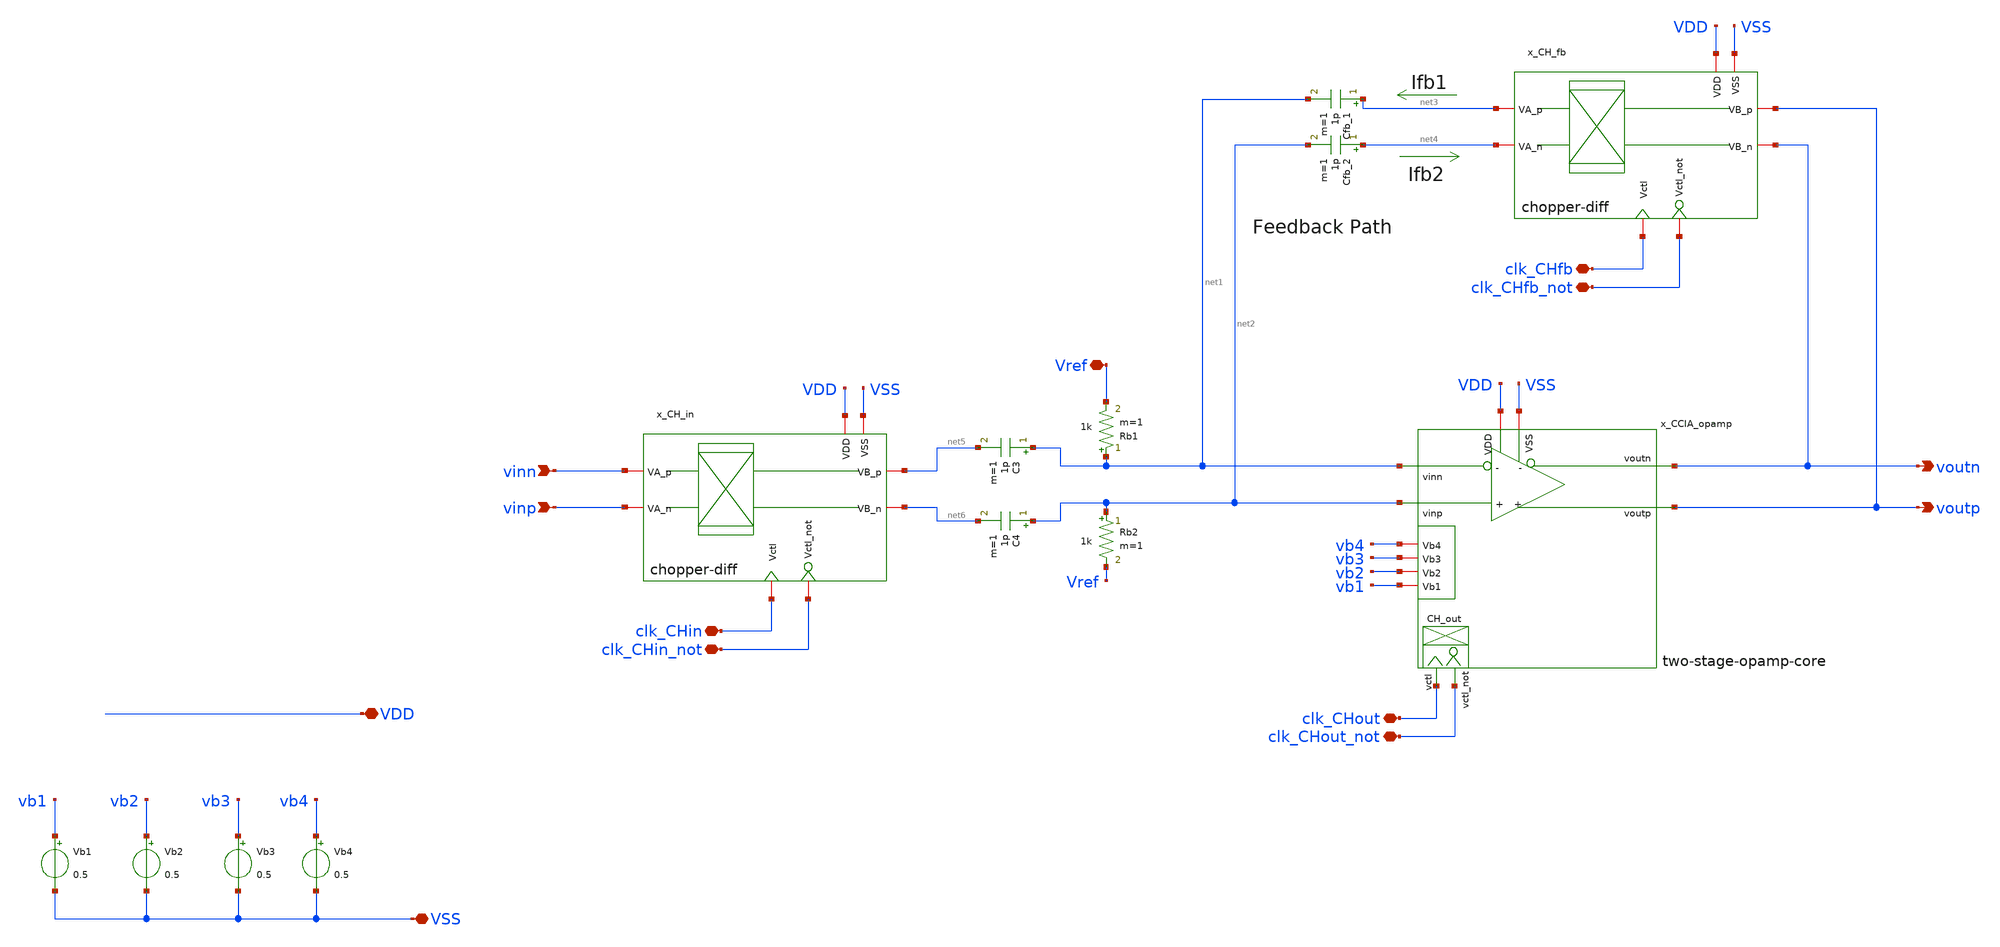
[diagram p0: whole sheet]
** sch_path: analog-db/circuits/ia_002_fan_chopper_simple/pdk/ihp-sg13g2/schematic/ccia-dut-chopper-simple.sch
* Copyright 2026 MacAnalog Research Group
**.subckt ccia-dut-chopper-simple VSS VDD voutn voutp clk_CHout clk_CHout_not clk_CHfb clk_CHfb_not
*+ clk_CHin clk_CHin_not vinn vinp Vref
*.iopin VSS
*.iopin VDD
*.opin voutn
*.opin voutp
*.iopin clk_CHout
*.iopin clk_CHout_not
*.iopin clk_CHfb
*.iopin clk_CHfb_not
*.iopin clk_CHin
*.iopin clk_CHin_not
*.ipin vinn
*.ipin vinp
*.iopin Vref
x_CCIA_opamp VDD vb4 net1 voutn vb3 net2 vb2 voutp clk_CHout clk_CHout_not vb1 VSS
+ two-stage-opamp-core
Vb1 vb1 VSS 0.5
Vb2 vb2 VSS 0.5
Vb3 vb3 VSS 0.5
x_CH_fb clk_CHfb VDD voutp net3 clk_CHfb_not VSS voutn net4 chopper-diff
Cfb_1 net3 net1 1p m=1
Cfb_2 net4 net2 1p m=1
C3 net1 net5 1p m=1
C4 net2 net6 1p m=1
x_CH_in clk_CHin VDD net5 vinn clk_CHin_not VSS net6 vinp chopper-diff
Rb1 net1 Vref 1k m=1
Rb2 net2 Vref 1k m=1
Vb4 vb4 VSS 0.5
**.ends
.end
